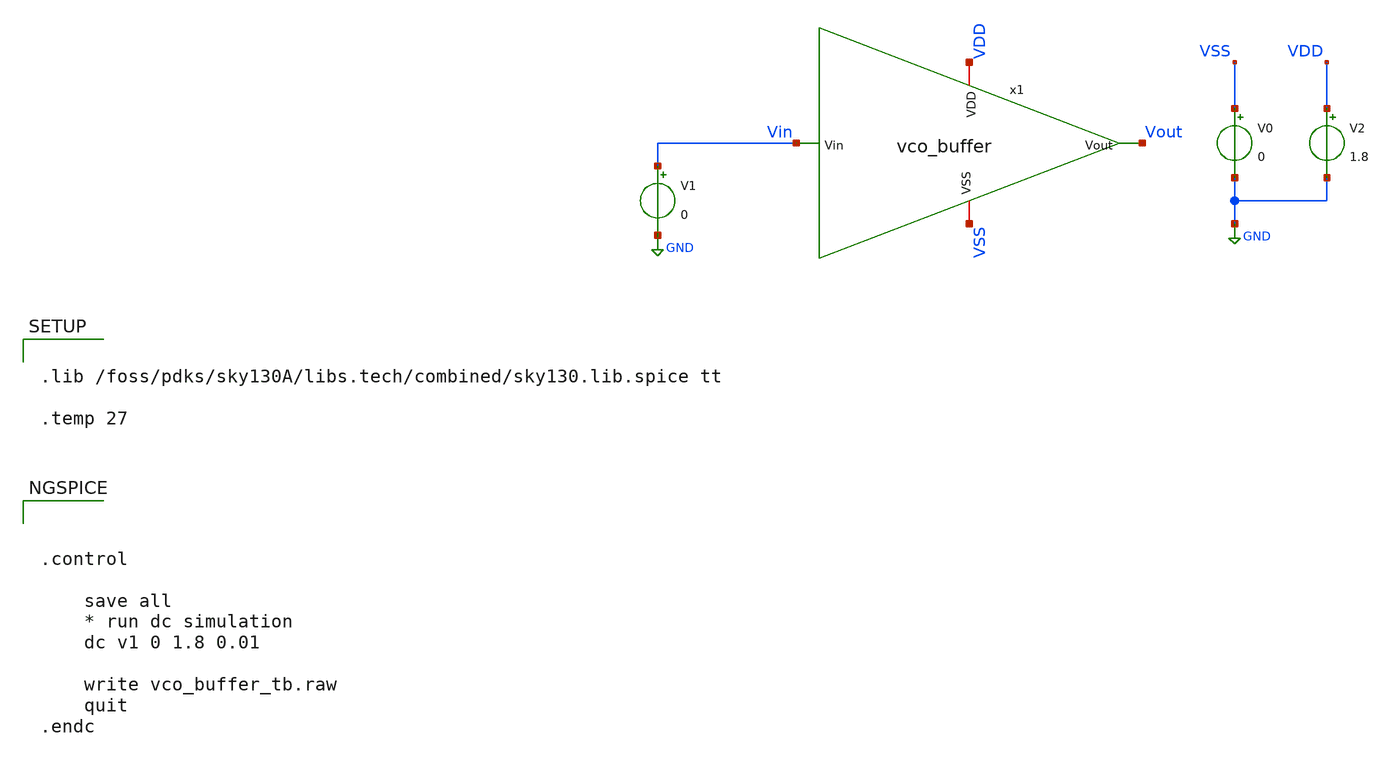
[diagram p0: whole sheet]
** sch_path: xschem/vco_buffer_tb.sch
**.subckt vco_buffer_tb
V0 VSS GND 0
V2 VDD GND 1.8
x1 VDD VSS Vin Vout vco_buffer
V1 Vin GND 0
**** begin user architecture code



.control

    save all
    * run dc simulation
    dc v1 0 1.8 0.01

    write vco_buffer_tb.raw
    quit
.endc




.lib /foss/pdks/sky130A/libs.tech/combined/sky130.lib.spice tt

.temp 27


**** end user architecture code
**.ends

* expanding   symbol:  vco_buffer.sym # of pins=4
** sym_path: xschem/vco_buffer.sym
** sch_path: xschem/vco_buffer.sch
.subckt vco_buffer VDD VSS Vin Vout
*.iopin VDD
*.iopin VSS
*.ipin Vin
*.opin Vout
x1 VDD Vin net1 VSS vco_inverter
x2 VDD net1 Vout VSS vco_inverter
.ends


* expanding   symbol:  vco_inverter.sym # of pins=4
** sym_path: xschem/vco_inverter.sym
** sch_path: xschem/vco_inverter.sch
.subckt vco_inverter VDD Vin Vout VSS
*.iopin VDD
*.iopin VSS
*.ipin Vin
*.opin Vout
XM1 Vout Vin VSS VSS sky130_fd_pr__nfet_01v8 L=0.15 W=1 nf=1 ad='int((nf+1)/2) * W/nf * 0.29' as='int((nf+2)/2) * W/nf * 0.29'
+ pd='2*int((nf+1)/2) * (W/nf + 0.29)' ps='2*int((nf+2)/2) * (W/nf + 0.29)' nrd='0.29 / W' nrs='0.29 / W'
+ sa=0 sb=0 sd=0 mult=1 m=1
XM2 Vout Vin VDD VDD sky130_fd_pr__pfet_01v8 L=0.15 W=1 nf=1 ad='int((nf+1)/2) * W/nf * 0.29' as='int((nf+2)/2) * W/nf * 0.29'
+ pd='2*int((nf+1)/2) * (W/nf + 0.29)' ps='2*int((nf+2)/2) * (W/nf + 0.29)' nrd='0.29 / W' nrs='0.29 / W'
+ sa=0 sb=0 sd=0 mult=1 m=1
.ends

.GLOBAL GND
.end
